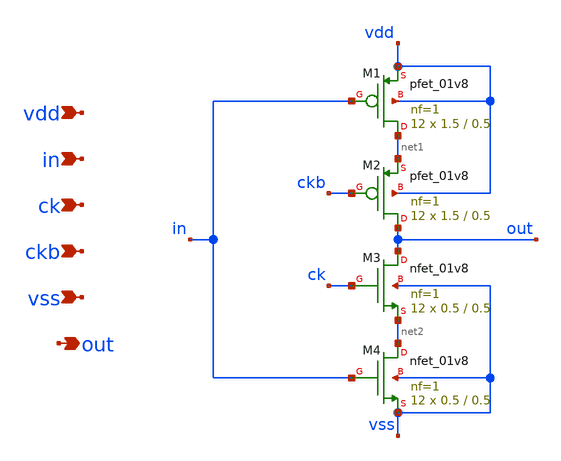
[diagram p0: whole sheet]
** sch_path: xschem/dac_sw_5.sch
**.subckt dac_sw_5 vdd in ck ckb vss out
*.ipin vdd
*.ipin in
*.ipin ck
*.ipin ckb
*.ipin vss
*.opin out
XM1 net1 in vdd vdd sky130_fd_pr__pfet_01v8 L=0.5 W=1.5 nf=1 ad='int((nf+1)/2) * W/nf * 0.29' as='int((nf+2)/2) * W/nf * 0.29'
+ pd='2*int((nf+1)/2) * (W/nf + 0.29)' ps='2*int((nf+2)/2) * (W/nf + 0.29)' nrd='0.29 / W' nrs='0.29 / W'
+ sa=0 sb=0 sd=0 mult=12 m=12
XM2 out ckb net1 vdd sky130_fd_pr__pfet_01v8 L=0.5 W=1.5 nf=1 ad='int((nf+1)/2) * W/nf * 0.29' as='int((nf+2)/2) * W/nf * 0.29'
+ pd='2*int((nf+1)/2) * (W/nf + 0.29)' ps='2*int((nf+2)/2) * (W/nf + 0.29)' nrd='0.29 / W' nrs='0.29 / W'
+ sa=0 sb=0 sd=0 mult=12 m=12
XM3 out ck net2 vss sky130_fd_pr__nfet_01v8 L=0.5 W=0.5 nf=1 ad='int((nf+1)/2) * W/nf * 0.29' as='int((nf+2)/2) * W/nf * 0.29'
+ pd='2*int((nf+1)/2) * (W/nf + 0.29)' ps='2*int((nf+2)/2) * (W/nf + 0.29)' nrd='0.29 / W' nrs='0.29 / W'
+ sa=0 sb=0 sd=0 mult=12 m=12
XM4 net2 in vss vss sky130_fd_pr__nfet_01v8 L=0.5 W=0.5 nf=1 ad='int((nf+1)/2) * W/nf * 0.29' as='int((nf+2)/2) * W/nf * 0.29'
+ pd='2*int((nf+1)/2) * (W/nf + 0.29)' ps='2*int((nf+2)/2) * (W/nf + 0.29)' nrd='0.29 / W' nrs='0.29 / W'
+ sa=0 sb=0 sd=0 mult=12 m=12
**.ends
.end
